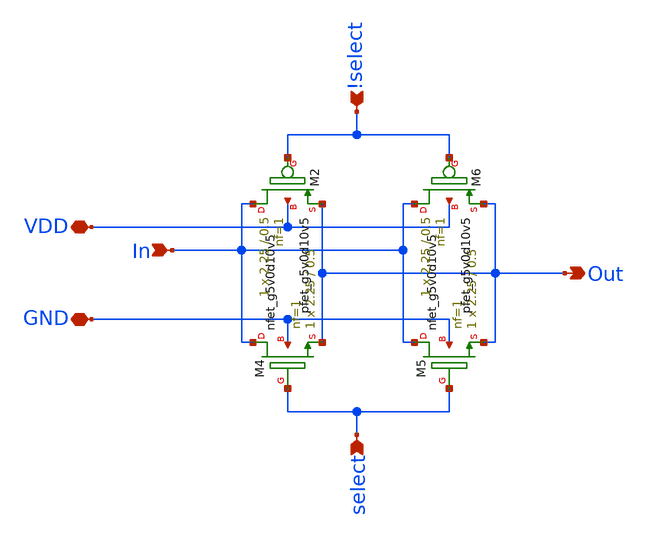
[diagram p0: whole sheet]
** sch_path: sky130_cells/Mux/Design/sky130_hilas_Tgate.sch
**.subckt sky130_hilas_Tgate In select !select VDD GND Out
*.ipin In
*.ipin select
*.ipin !select
*.iopin VDD
*.iopin GND
*.opin Out
XM4 In select Out GND sky130_fd_pr__nfet_g5v0d10v5 L=0.5 W=2.25 nf=1 ad='int((nf+1)/2) * W/nf * 0.29'
+ as='int((nf+2)/2) * W/nf * 0.29' pd='2*int((nf+1)/2) * (W/nf + 0.29)' ps='2*int((nf+2)/2) * (W/nf + 0.29)'
+ nrd='0.29 / W' nrs='0.29 / W' sa=0 sb=0 sd=0 mult=1 m=1
XM2 In !select Out VDD sky130_fd_pr__pfet_g5v0d10v5 L=0.5 W=2.25 nf=1 ad='int((nf+1)/2) * W/nf * 0.29'
+ as='int((nf+2)/2) * W/nf * 0.29' pd='2*int((nf+1)/2) * (W/nf + 0.29)' ps='2*int((nf+2)/2) * (W/nf + 0.29)'
+ nrd='0.29 / W' nrs='0.29 / W' sa=0 sb=0 sd=0 mult=1 m=1
XM5 In select Out GND sky130_fd_pr__nfet_g5v0d10v5 L=0.5 W=2.25 nf=1 ad='int((nf+1)/2) * W/nf * 0.29'
+ as='int((nf+2)/2) * W/nf * 0.29' pd='2*int((nf+1)/2) * (W/nf + 0.29)' ps='2*int((nf+2)/2) * (W/nf + 0.29)'
+ nrd='0.29 / W' nrs='0.29 / W' sa=0 sb=0 sd=0 mult=1 m=1
XM6 In !select Out VDD sky130_fd_pr__pfet_g5v0d10v5 L=0.5 W=2.25 nf=1 ad='int((nf+1)/2) * W/nf * 0.29'
+ as='int((nf+2)/2) * W/nf * 0.29' pd='2*int((nf+1)/2) * (W/nf + 0.29)' ps='2*int((nf+2)/2) * (W/nf + 0.29)'
+ nrd='0.29 / W' nrs='0.29 / W' sa=0 sb=0 sd=0 mult=1 m=1
**.ends
.end
